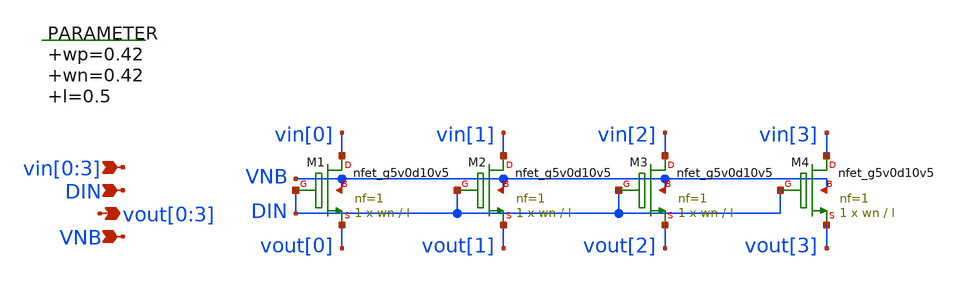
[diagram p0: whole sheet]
** sch_path: xschem/switch_nmos_1g_4o.sch
**.subckt switch_nmos_1g_4o vin[0],vin[1],vin[2],vin[3] vout[0],vout[1],vout[2],vout[3] VNB DIN
*.ipin vin[0],vin[1],vin[2],vin[3]
*.opin vout[0],vout[1],vout[2],vout[3]
*.ipin VNB
*.ipin DIN
.param wp=0.42 wn=0.42 l=0.5

XM1 vin[0] DIN vout[0] VNB sky130_fd_pr__nfet_g5v0d10v5 L=l W=wn nf=1 ad='int((nf+1)/2) * W/nf * 0.29'
+ as='int((nf+2)/2) * W/nf * 0.29' pd='2*int((nf+1)/2) * (W/nf + 0.29)' ps='2*int((nf+2)/2) * (W/nf + 0.29)'
+ nrd='0.29 / W' nrs='0.29 / W' sa=0 sb=0 sd=0 mult=1 m=1
XM2 vin[1] DIN vout[1] VNB sky130_fd_pr__nfet_g5v0d10v5 L=l W=wn nf=1 ad='int((nf+1)/2) * W/nf * 0.29'
+ as='int((nf+2)/2) * W/nf * 0.29' pd='2*int((nf+1)/2) * (W/nf + 0.29)' ps='2*int((nf+2)/2) * (W/nf + 0.29)'
+ nrd='0.29 / W' nrs='0.29 / W' sa=0 sb=0 sd=0 mult=1 m=1
XM3 vin[2] DIN vout[2] VNB sky130_fd_pr__nfet_g5v0d10v5 L=l W=wn nf=1 ad='int((nf+1)/2) * W/nf * 0.29'
+ as='int((nf+2)/2) * W/nf * 0.29' pd='2*int((nf+1)/2) * (W/nf + 0.29)' ps='2*int((nf+2)/2) * (W/nf + 0.29)'
+ nrd='0.29 / W' nrs='0.29 / W' sa=0 sb=0 sd=0 mult=1 m=1
XM4 vin[3] DIN vout[3] VNB sky130_fd_pr__nfet_g5v0d10v5 L=l W=wn nf=1 ad='int((nf+1)/2) * W/nf * 0.29'
+ as='int((nf+2)/2) * W/nf * 0.29' pd='2*int((nf+1)/2) * (W/nf + 0.29)' ps='2*int((nf+2)/2) * (W/nf + 0.29)'
+ nrd='0.29 / W' nrs='0.29 / W' sa=0 sb=0 sd=0 mult=1 m=1
**.ends
.end
